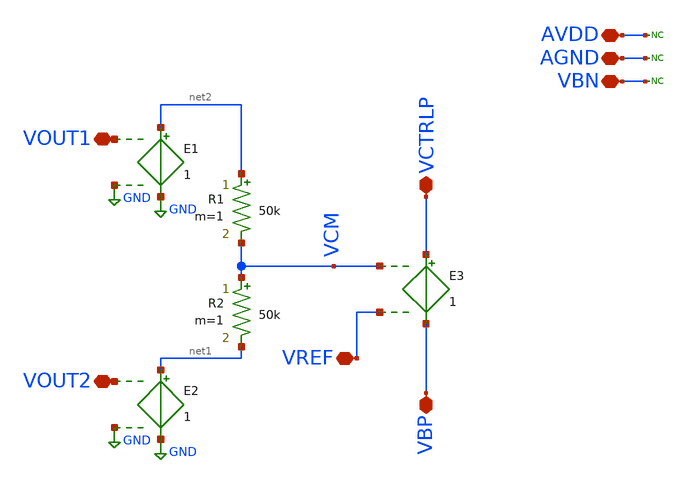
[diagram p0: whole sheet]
** sch_path: ITI_Labs/Lab11_Xschem/Design/CMFB_Behav.sch
**.subckt CMFB_Behav VOUT1 VOUT2 VREF VCTRLP VBP AVDD AGND VBN
*.iopin VOUT1
*.iopin VOUT2
*.iopin VREF
*.iopin VCTRLP
*.iopin VBP
*.iopin AVDD
*.iopin AGND
*.iopin VBN
E1 net2 GND VOUT1 GND 1
E2 net1 GND VOUT2 GND 1
E3 VCTRLP VBP VCM VREF 1
R1 net2 VCM 50k m=1
R2 VCM net1 50k m=1
* noconn AVDD
* noconn AGND
* noconn VBN
**.ends
.GLOBAL GND
.end
